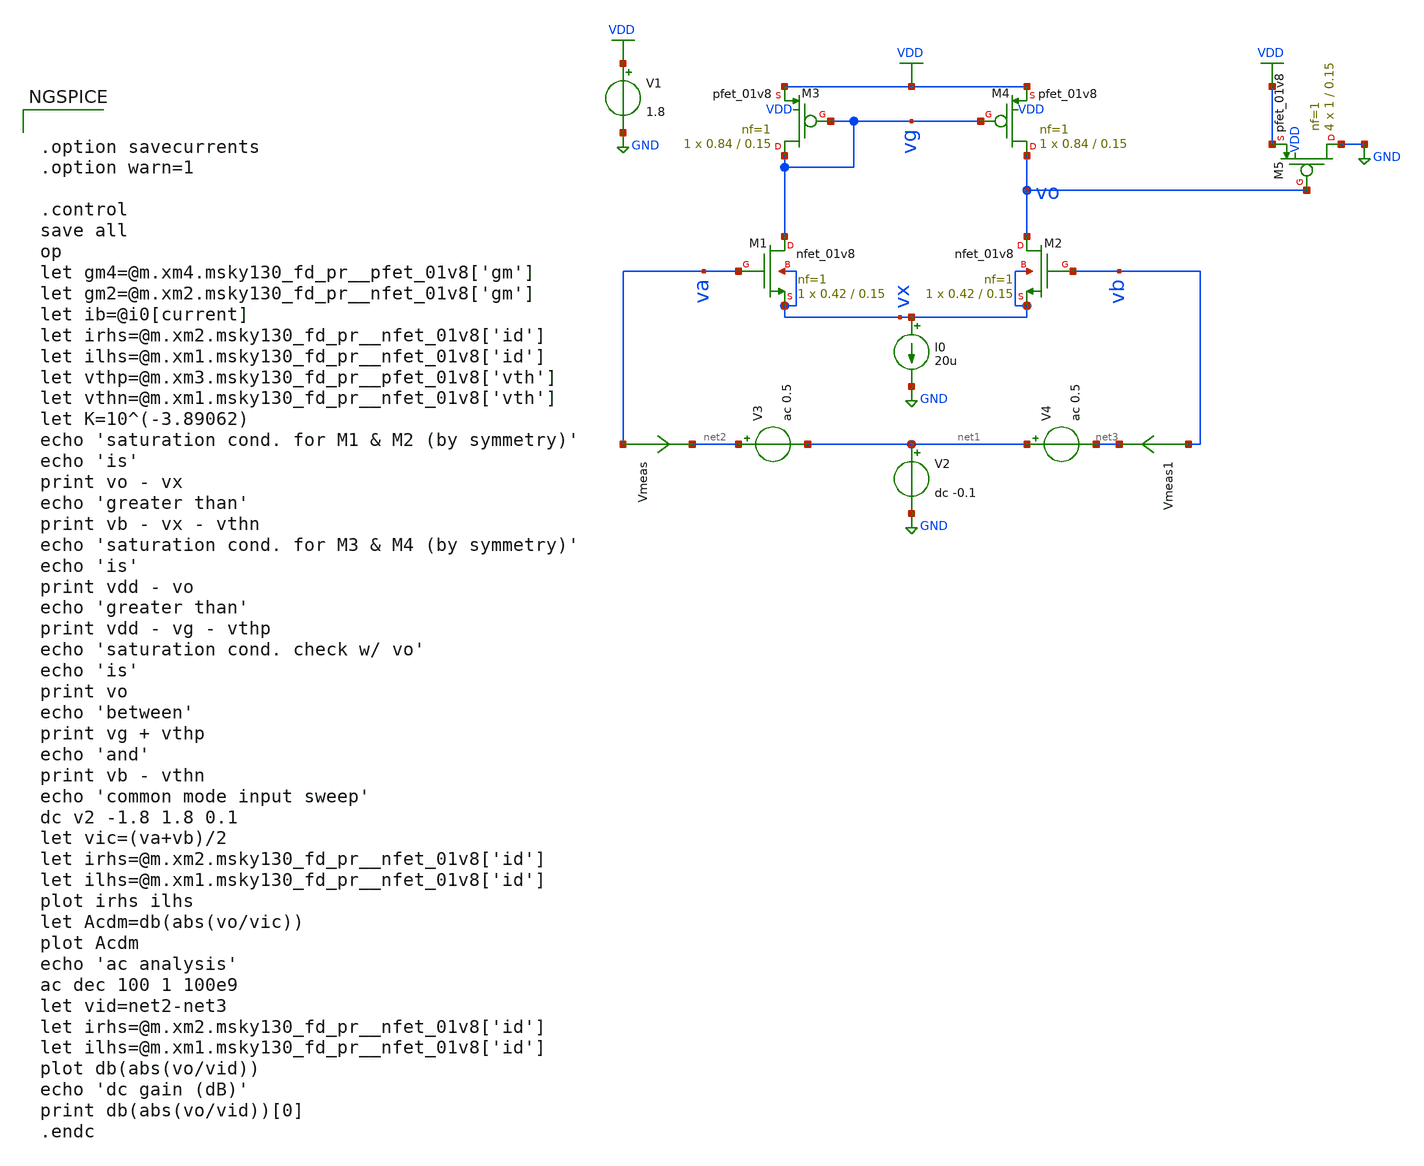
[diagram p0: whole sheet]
** sch_path: schematics/amplifier.sch
**.subckt amplifier
XM4 vo vg VDD VDD sky130_fd_pr__pfet_01v8 L=0.15 W=0.84 nf=1 ad='int((nf+1)/2) * W/nf * 0.29' as='int((nf+2)/2) * W/nf * 0.29'
+ pd='2*int((nf+1)/2) * (W/nf + 0.29)' ps='2*int((nf+2)/2) * (W/nf + 0.29)' nrd='0.29 / W' nrs='0.29 / W'
+ sa=0 sb=0 sd=0 mult=1 m=1
I0 vx GND 20u
V1 VDD GND 1.8
V2 net1 GND dc -0.1
Vmeas va net2 0
.save i(vmeas)
Vmeas1 vb net3 0
.save i(vmeas1)
XM2 vo vb vx vx sky130_fd_pr__nfet_01v8 L=0.15 W=0.42 nf=1 ad='int((nf+1)/2) * W/nf * 0.29' as='int((nf+2)/2) * W/nf * 0.29'
+ pd='2*int((nf+1)/2) * (W/nf + 0.29)' ps='2*int((nf+2)/2) * (W/nf + 0.29)' nrd='0.29 / W' nrs='0.29 / W'
+ sa=0 sb=0 sd=0 mult=1 m=1
XM1 vg va vx vx sky130_fd_pr__nfet_01v8 L=0.15 W=0.42 nf=1 ad='int((nf+1)/2) * W/nf * 0.29' as='int((nf+2)/2) * W/nf * 0.29'
+ pd='2*int((nf+1)/2) * (W/nf + 0.29)' ps='2*int((nf+2)/2) * (W/nf + 0.29)' nrd='0.29 / W' nrs='0.29 / W'
+ sa=0 sb=0 sd=0 mult=1 m=1
XM3 vg vg VDD VDD sky130_fd_pr__pfet_01v8 L=0.15 W=0.84 nf=1 ad='int((nf+1)/2) * W/nf * 0.29' as='int((nf+2)/2) * W/nf * 0.29'
+ pd='2*int((nf+1)/2) * (W/nf + 0.29)' ps='2*int((nf+2)/2) * (W/nf + 0.29)' nrd='0.29 / W' nrs='0.29 / W'
+ sa=0 sb=0 sd=0 mult=1 m=1
XM5 GND vo VDD VDD sky130_fd_pr__pfet_01v8 L=0.15 W=1 nf=1 ad='int((nf+1)/2) * W/nf * 0.29' as='int((nf+2)/2) * W/nf * 0.29'
+ pd='2*int((nf+1)/2) * (W/nf + 0.29)' ps='2*int((nf+2)/2) * (W/nf + 0.29)' nrd='0.29 / W' nrs='0.29 / W'
+ sa=0 sb=0 sd=0 mult=4 m=4
V3 net2 net1 ac 0.5
V4 net1 net3 ac 0.5
**** begin user architecture code


.option savecurrents
.option warn=1

.control
save all
op
let gm4=@m.xm4.msky130_fd_pr__pfet_01v8['gm']
let gm2=@m.xm2.msky130_fd_pr__nfet_01v8['gm']
let ib=@i0[current]
let irhs=@m.xm2.msky130_fd_pr__nfet_01v8['id']
let ilhs=@m.xm1.msky130_fd_pr__nfet_01v8['id']
let vthp=@m.xm3.msky130_fd_pr__pfet_01v8['vth']
let vthn=@m.xm1.msky130_fd_pr__nfet_01v8['vth']
let K=10^(-3.89062)
echo 'saturation cond. for M1 & M2 (by symmetry)'
echo 'is'
print vo - vx
echo 'greater than'
print vb - vx - vthn
echo 'saturation cond. for M3 & M4 (by symmetry)'
echo 'is'
print vdd - vo
echo 'greater than'
print vdd - vg - vthp
echo 'saturation cond. check w/ vo'
echo 'is'
print vo
echo 'between'
print vg + vthp
echo 'and'
print vb - vthn
echo 'common mode input sweep'
dc v2 -1.8 1.8 0.1
let vic=(va+vb)/2
let irhs=@m.xm2.msky130_fd_pr__nfet_01v8['id']
let ilhs=@m.xm1.msky130_fd_pr__nfet_01v8['id']
plot irhs ilhs
let Acdm=db(abs(vo/vic))
plot Acdm
echo 'ac analysis'
ac dec 100 1 100e9
let vid=net2-net3
let irhs=@m.xm2.msky130_fd_pr__nfet_01v8['id']
let ilhs=@m.xm1.msky130_fd_pr__nfet_01v8['id']
plot db(abs(vo/vid))
echo 'dc gain (dB)'
print db(abs(vo/vid))[0]
.endc



.include $::SKYWATER_MODELS/cells/nfet_01v8/sky130_fd_pr__nfet_01v8__tt.corner.spice
.include $::SKYWATER_MODELS/cells/nfet_01v8_lvt/sky130_fd_pr__nfet_01v8_lvt__tt.corner.spice
.include $::SKYWATER_MODELS/cells/pfet_01v8/sky130_fd_pr__pfet_01v8__tt.corner.spice
.include $::SKYWATER_MODELS/cells/nfet_03v3_nvt/sky130_fd_pr__nfet_03v3_nvt__tt.corner.spice
.include $::SKYWATER_MODELS/cells/nfet_05v0_nvt/sky130_fd_pr__nfet_05v0_nvt__tt.corner.spice
.include $::SKYWATER_MODELS/cells/esd_nfet_01v8/sky130_fd_pr__esd_nfet_01v8__tt.corner.spice
.include $::SKYWATER_MODELS/cells/pfet_01v8_lvt/sky130_fd_pr__pfet_01v8_lvt__tt.corner.spice
.include $::SKYWATER_MODELS/cells/pfet_01v8_hvt/sky130_fd_pr__pfet_01v8_hvt__tt.corner.spice
.include $::SKYWATER_MODELS/cells/esd_pfet_g5v0d10v5/sky130_fd_pr__esd_pfet_g5v0d10v5__tt.corner.spice
.include $::SKYWATER_MODELS/cells/pfet_g5v0d10v5/sky130_fd_pr__pfet_g5v0d10v5__tt.corner.spice
.include $::SKYWATER_MODELS/cells/pfet_g5v0d16v0/sky130_fd_pr__pfet_g5v0d16v0__tt.corner.spice
.include $::SKYWATER_MODELS/cells/nfet_g5v0d10v5/sky130_fd_pr__nfet_g5v0d10v5__tt.corner.spice
.include $::SKYWATER_MODELS/cells/nfet_g5v0d16v0/sky130_fd_pr__nfet_g5v0d16v0__tt_discrete.corner.spice
.include $::SKYWATER_MODELS/cells/esd_nfet_g5v0d10v5/sky130_fd_pr__esd_nfet_g5v0d10v5__tt.corner.spice
.include $::SKYWATER_MODELS/models/corners/tt/nonfet.spice
* Mismatch parameters
.include $::SKYWATER_MODELS/cells/nfet_01v8/sky130_fd_pr__nfet_01v8__mismatch.corner.spice
.include $::SKYWATER_MODELS/cells/pfet_01v8/sky130_fd_pr__pfet_01v8__mismatch.corner.spice
.include $::SKYWATER_MODELS/cells/nfet_01v8_lvt/sky130_fd_pr__nfet_01v8_lvt__mismatch.corner.spice
.include $::SKYWATER_MODELS/cells/pfet_01v8_lvt/sky130_fd_pr__pfet_01v8_lvt__mismatch.corner.spice
.include $::SKYWATER_MODELS/cells/pfet_01v8_hvt/sky130_fd_pr__pfet_01v8_hvt__mismatch.corner.spice
.include $::SKYWATER_MODELS/cells/nfet_g5v0d10v5/sky130_fd_pr__nfet_g5v0d10v5__mismatch.corner.spice
.include $::SKYWATER_MODELS/cells/pfet_g5v0d10v5/sky130_fd_pr__pfet_g5v0d10v5__mismatch.corner.spice
.include $::SKYWATER_MODELS/cells/nfet_05v0_nvt/sky130_fd_pr__nfet_05v0_nvt__mismatch.corner.spice
.include $::SKYWATER_MODELS/cells/nfet_03v3_nvt/sky130_fd_pr__nfet_03v3_nvt__mismatch.corner.spice
* Resistor$::SKYWATER_MODELS/Capacitor
.include $::SKYWATER_MODELS/models/r+c/res_typical__cap_typical.spice
.include $::SKYWATER_MODELS/models/r+c/res_typical__cap_typical__lin.spice
* Special cells
.include $::SKYWATER_MODELS/models/corners/tt/specialized_cells.spice
* All models
.include $::SKYWATER_MODELS/models/all.spice
.include $::SKYWATER_MODELS/cells/pnp_05v5/sky130_fd_pr__pnp_05v5_W3p40L3p40.model.spice
* Corner
.include $::SKYWATER_MODELS/models/corners/tt/rf.spice

**** end user architecture code
**.ends
.GLOBAL GND
.GLOBAL VDD
.end
